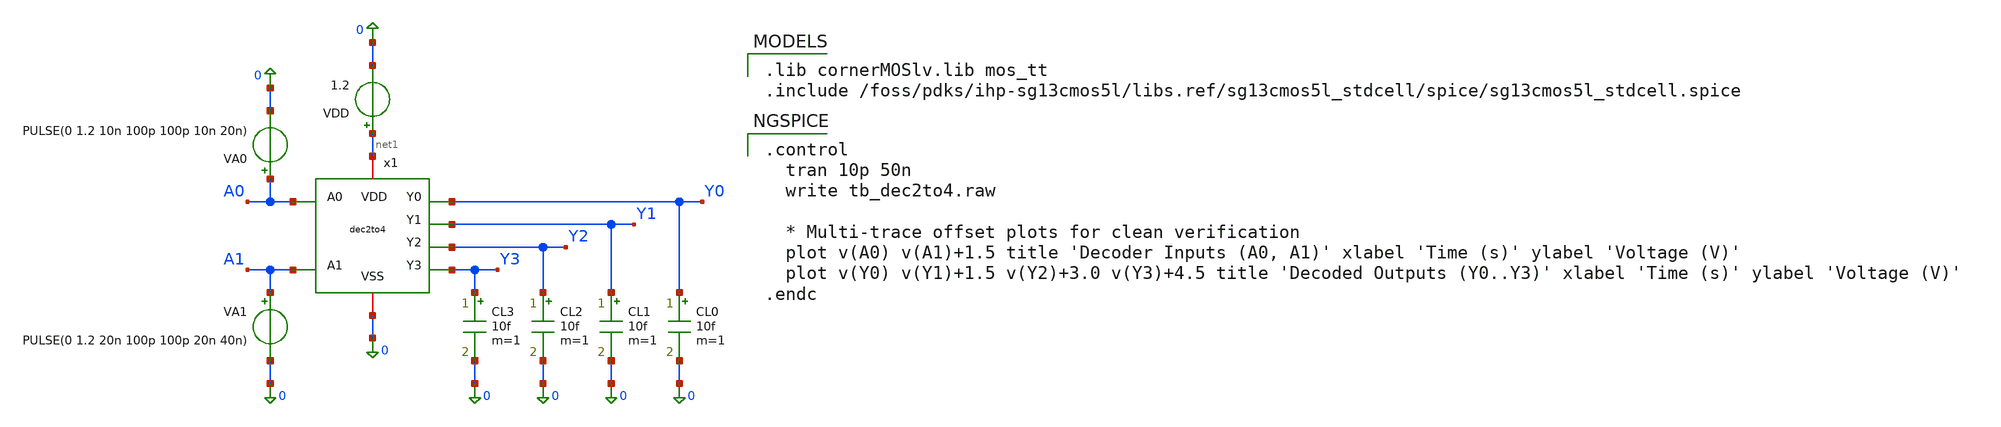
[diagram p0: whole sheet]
** sch_path: archives/dec2to4/tb_dec2to4.sch
**.subckt tb_dec2to4
CL3 Y3 0 10f m=1
CL2 Y2 0 10f m=1
CL1 Y1 0 10f m=1
CL0 Y0 0 10f m=1
VDD net1 0 1.2
VA1 A1 0 PULSE(0 1.2 20n 100p 100p 20n 40n)
VA0 A0 0 PULSE(0 1.2 10n 100p 100p 10n 20n)
x1 A0 A1 Y0 Y1 Y2 Y3 net1 0 dec2to4
**** begin user architecture code

.lib cornerMOSlv.lib mos_tt
.include /foss/pdks/ihp-sg13cmos5l/libs.ref/sg13cmos5l_stdcell/spice/sg13cmos5l_stdcell.spice


.control
  tran 10p 50n
  write tb_dec2to4.raw

  * Multi-trace offset plots for clean verification
  plot v(A0) v(A1)+1.5 title 'Decoder Inputs (A0, A1)' xlabel 'Time (s)' ylabel 'Voltage (V)'
  plot v(Y0) v(Y1)+1.5 v(Y2)+3.0 v(Y3)+4.5 title 'Decoded Outputs (Y0..Y3)' xlabel 'Time (s)' ylabel
+ 'Voltage (V)'
.endc

**** end user architecture code
**.ends
.end
